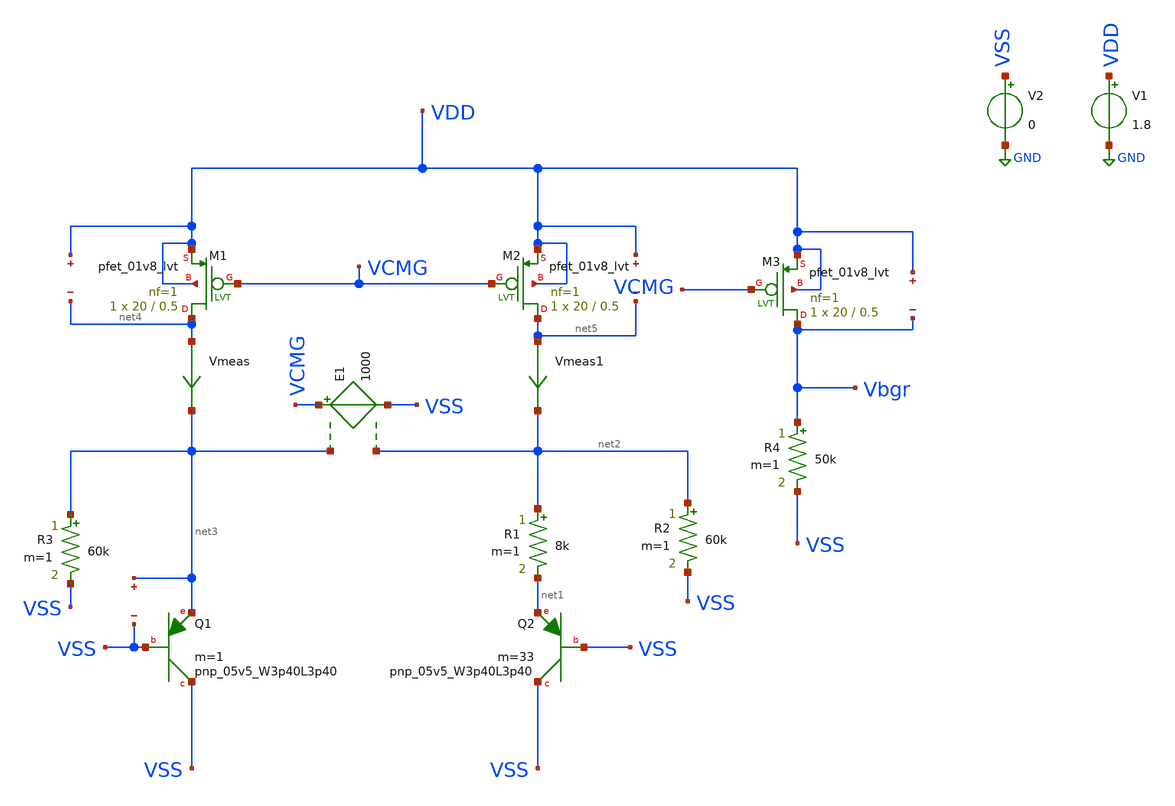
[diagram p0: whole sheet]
** sch_path: custom_gds/tt_um_bgr_agolmanesh/xschem/idealBGRCore_old.sch
**.subckt idealBGRCore_old
XQ1 VSS VSS net3 sky130_fd_pr__pnp_05v5_W3p40L3p40 m=1
XQ2 VSS VSS net1 sky130_fd_pr__pnp_05v5_W3p40L3p40 m=33
XM1 net4 VCMG VDD VDD sky130_fd_pr__pfet_01v8_lvt L=0.5 W=20 nf=1 ad='int((nf+1)/2) * W/nf * 0.29' as='int((nf+2)/2) * W/nf * 0.29'
+ pd='2*int((nf+1)/2) * (W/nf + 0.29)' ps='2*int((nf+2)/2) * (W/nf + 0.29)' nrd='0.29 / W' nrs='0.29 / W'
+ sa=0 sb=0 sd=0 mult=1 m=1
XM2 net5 VCMG VDD VDD sky130_fd_pr__pfet_01v8_lvt L=0.5 W=20 nf=1 ad='int((nf+1)/2) * W/nf * 0.29' as='int((nf+2)/2) * W/nf * 0.29'
+ pd='2*int((nf+1)/2) * (W/nf + 0.29)' ps='2*int((nf+2)/2) * (W/nf + 0.29)' nrd='0.29 / W' nrs='0.29 / W'
+ sa=0 sb=0 sd=0 mult=1 m=1
XM3 Vbgr VCMG VDD VDD sky130_fd_pr__pfet_01v8_lvt L=0.5 W=20 nf=1 ad='int((nf+1)/2) * W/nf * 0.29' as='int((nf+2)/2) * W/nf * 0.29'
+ pd='2*int((nf+1)/2) * (W/nf + 0.29)' ps='2*int((nf+2)/2) * (W/nf + 0.29)' nrd='0.29 / W' nrs='0.29 / W'
+ sa=0 sb=0 sd=0 mult=1 m=1
E1 VCMG VSS net3 net2 1000
R1 net2 net1 8k m=1
R2 net2 VSS 60k m=1
R3 net3 VSS 60k m=1
R4 Vbgr VSS 50k m=1
V1 VDD GND 1.8
V2 VSS GND 0
Vmeas net4 net3 0
.save i(vmeas)
Vmeas1 net5 net2 0
.save i(vmeas1)
.save v(vdd)
.save v(net4)
.save v(vdd)
.save v(net5)
.save v(vdd)
.save v(vbgr)
.save v(net3)
.save v(vss)
**** begin user architecture code

** opencircuitdesign pdks install
.lib $::SKYWATER_MODELS/sky130.lib.spice tt


**** end user architecture code
**.ends
.GLOBAL GND
**** begin user architecture code



.control
op
save all


.endc



**** end user architecture code
.end
